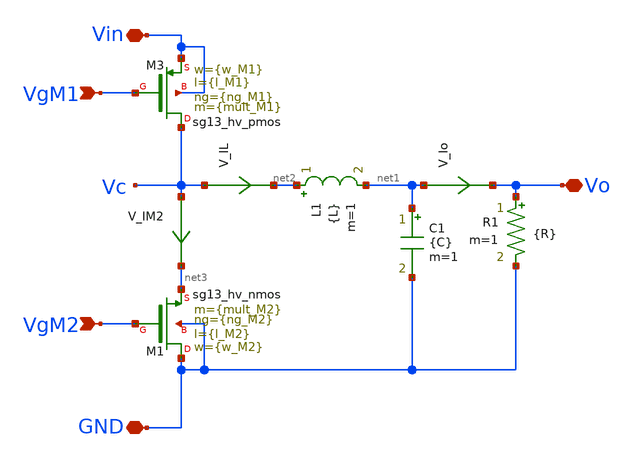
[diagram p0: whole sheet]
** sch_path: xschem/Ayudantias/Ayudantia_1/DCDC_Buck.sch
**.subckt DCDC_Buck Vin VgM1 VgM2 Vo GND
*.iopin Vin
*.ipin VgM1
*.ipin VgM2
*.iopin Vo
*.iopin GND
L1 net2 net1 {L} m=1
C1 net1 GND {C} m=1
V_Io net1 Vo 0
.save i(v_io)
V_IL Vc net2 0
.save i(v_il)
R1 Vo GND {R} m=1
V_IM2 Vc net3 0
.save i(v_im2)
XM3 Vc VgM1 Vin Vin sg13_hv_pmos w={w_M1} l={l_M1} ng={ng_M1} m={mult_M1} mm_ok=1
XM1 GND VgM2 net3 GND sg13_hv_nmos w={w_M2} l={l_M2} ng={ng_M2} m={mult_M2} mm_ok=1
**.ends
.end
